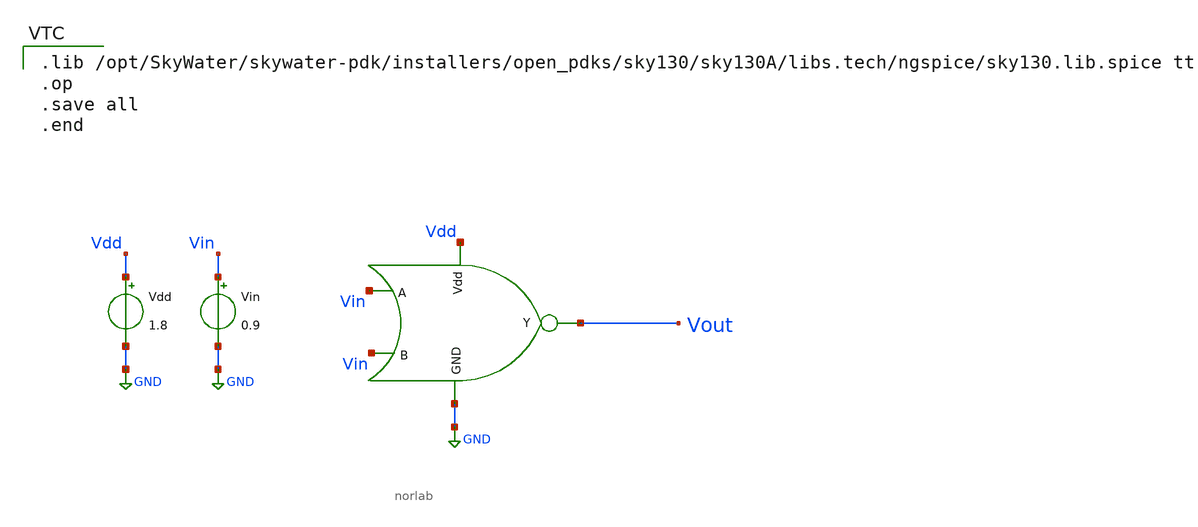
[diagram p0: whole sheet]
** sch_path: 2/src/nor_test.sch
**.subckt nor_test
Vdd Vdd GND 1.8
.save i(vdd)
Vin Vin GND 0.9
.save i(vin)
x2 Vdd Vin Vin Vout GND norlab
**** begin user architecture code

.lib /opt/SkyWater/skywater-pdk/installers/open_pdks/sky130/sky130A/libs.tech/ngspice/sky130.lib.spice tt
.op
.save all
.end

**** end user architecture code
**.ends
.GLOBAL GND
.end
